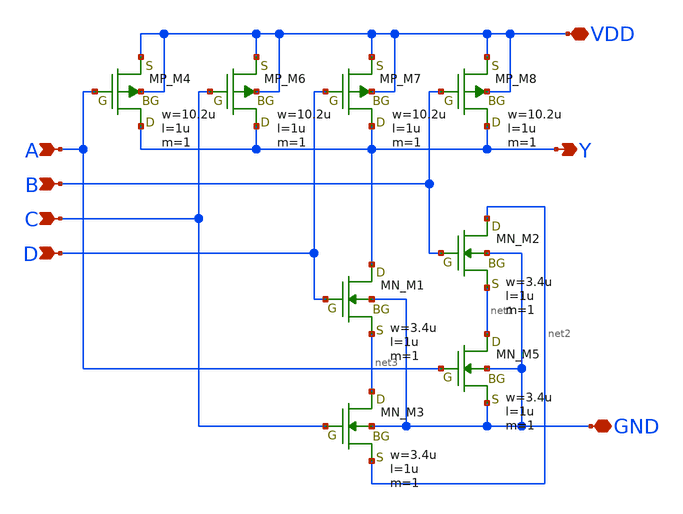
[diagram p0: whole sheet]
** sch_path: libs.tech/xschem/TR-1um_stdcell/NAND4.sch
**.subckt NAND4 B A Y GND VDD D C
*.ipin B
*.ipin A
*.opin Y
*.iopin GND
*.iopin VDD
*.ipin D
*.ipin C
XM4 Y A VDD VDD PMOS w=10.2u l=1u nrd=0 nrs=0 m=1
XM6 Y C VDD VDD PMOS w=10.2u l=1u nrd=0 nrs=0 m=1
XM7 Y D VDD VDD PMOS w=10.2u l=1u nrd=0 nrs=0 m=1
XM8 Y B VDD VDD PMOS w=10.2u l=1u nrd=0 nrs=0 m=1
XM1 Y D net3 GND NMOS w=3.4u l=1u nrd=0 nrs=0 m=1
XM2 net2 B net1 GND NMOS w=3.4u l=1u nrd=0 nrs=0 m=1
XM3 net3 C net2 GND NMOS w=3.4u l=1u nrd=0 nrs=0 m=1
XM5 net1 A GND GND NMOS w=3.4u l=1u nrd=0 nrs=0 m=1
**.ends
.end
